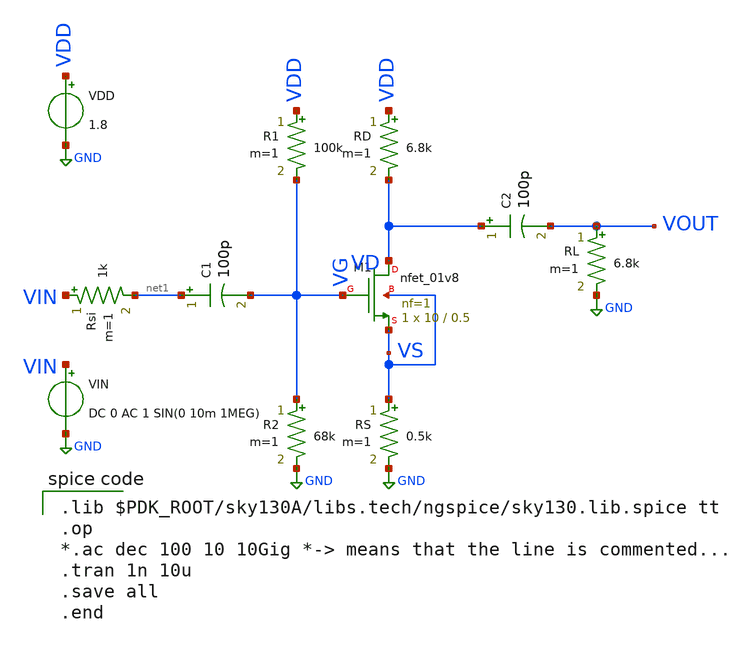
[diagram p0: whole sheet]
** sch_path: nmos_common_source_amplifier/schematic/cs_amplifier.sch
**.subckt cs_amplifier
XM1 VD VG VS VS sky130_fd_pr__nfet_01v8 L=0.5 W=10 nf=1 ad='int((1 + 1)/2) * 10 / 1 * 0.29' as='int((1 + 2)/2) * 10 / 1 * 0.29'
+ pd='2*int((1 + 1)/2) * (10 / 1 + 0.29)' ps='2*int((1 + 2)/2) * (10 / 1 + 0.29)' nrd='0.29 / 10 ' nrs='0.29 / 10 '
+ sa=0 sb=0 sd=0 mult=1 m=1
RS VS GND 0.5k m=1
C1 net1 VG 100p m=1
VIN VIN GND DC 0 AC 1 SIN(0 10m 1MEG)
Rsi VIN net1 1k m=1
R1 VDD VG 100k m=1
R2 VG GND 68k m=1
RD VDD VD 6.8k m=1
RL VOUT GND 6.8k m=1
C2 VD VOUT 100p m=1
VDD VDD GND 1.8
**** begin user architecture code

.lib $PDK_ROOT/sky130A/libs.tech/ngspice/sky130.lib.spice tt
.op
*.ac dec 100 10 10Gig *-> means that the line is commented...
.tran 1n 10u
.save all
.end

**** end user architecture code
**.ends
.GLOBAL GND
.end
